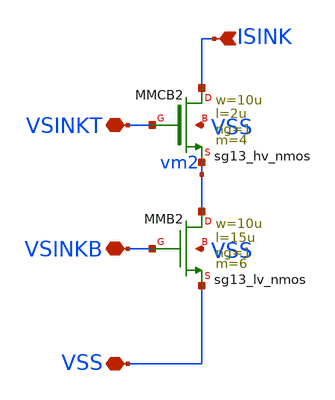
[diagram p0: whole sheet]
** sch_path: ip/vthref/xschem/vthref_sink.sch
**.subckt vthref_sink VSS ISINK VSINKT VSINKB
*.iopin VSS
*.ipin ISINK
*.iopin VSINKT
*.iopin VSINKB
XMMCB2 ISINK VSINKT vm2 VSS sg13_hv_nmos w=10u l=2u ng=1 m=4 mm_ok=1
XMMB2 vm2 VSINKB VSS VSS sg13_lv_nmos w=10u l=15u ng=1 m=6 mm_ok=1
**.ends
.end
